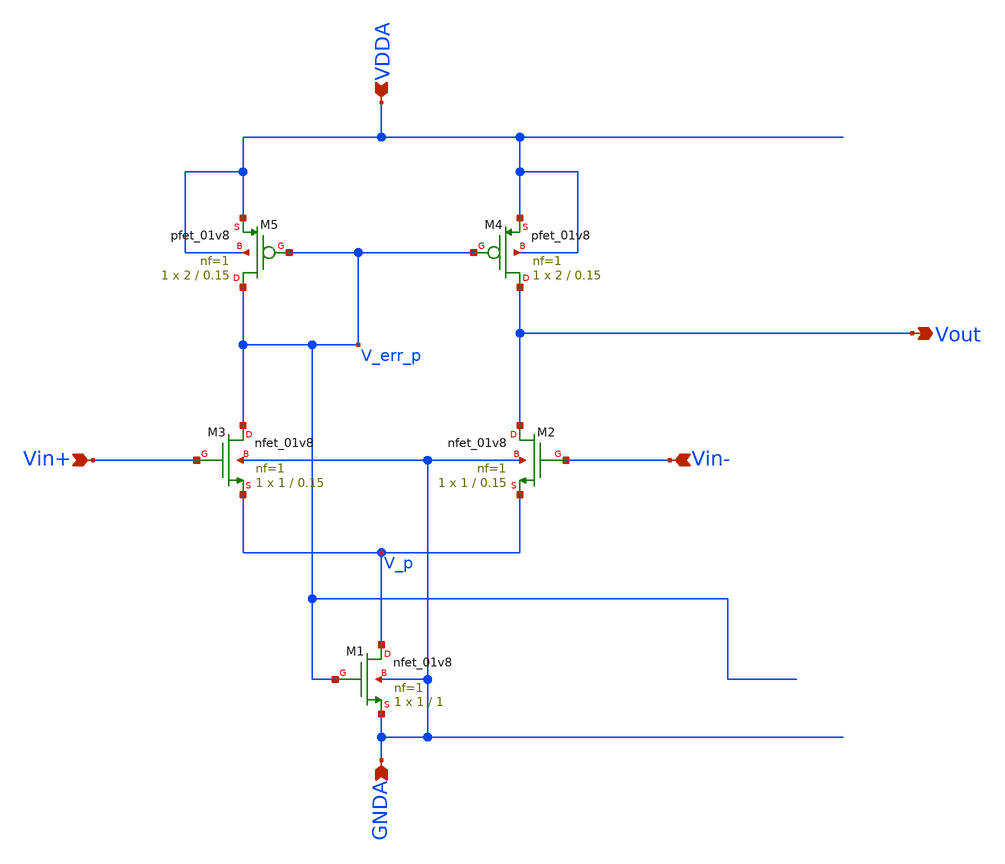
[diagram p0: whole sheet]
** sch_path: projects/bandgapref/xschem_ngspice/new_files/opamp_bandgap_4.sch
**.subckt opamp_bandgap_4 Vin+ Vout Vin- GNDA VDDA
*.ipin Vin+
*.opin Vout
*.ipin Vin-
*.ipin GNDA
*.ipin VDDA
XM4 Vout V_err_p VDDA VDDA sky130_fd_pr__pfet_01v8 L=0.15 W=2 nf=1 ad='int((nf+1)/2) * W/nf * 0.29' as='int((nf+2)/2) * W/nf * 0.29'
+ pd='2*int((nf+1)/2) * (W/nf + 0.29)' ps='2*int((nf+2)/2) * (W/nf + 0.29)' nrd='0.29 / W' nrs='0.29 / W'
+ sa=0 sb=0 sd=0 mult=1 m=1
XM5 V_err_p V_err_p VDDA VDDA sky130_fd_pr__pfet_01v8 L=0.15 W=2 nf=1 ad='int((nf+1)/2) * W/nf * 0.29'
+ as='int((nf+2)/2) * W/nf * 0.29' pd='2*int((nf+1)/2) * (W/nf + 0.29)' ps='2*int((nf+2)/2) * (W/nf + 0.29)'
+ nrd='0.29 / W' nrs='0.29 / W' sa=0 sb=0 sd=0 mult=1 m=1
XM2 Vout Vin- V_p GNDA sky130_fd_pr__nfet_01v8 L=0.15 W=1 nf=1 ad='int((nf+1)/2) * W/nf * 0.29' as='int((nf+2)/2) * W/nf * 0.29'
+ pd='2*int((nf+1)/2) * (W/nf + 0.29)' ps='2*int((nf+2)/2) * (W/nf + 0.29)' nrd='0.29 / W' nrs='0.29 / W'
+ sa=0 sb=0 sd=0 mult=1 m=1
XM3 V_err_p Vin+ V_p GNDA sky130_fd_pr__nfet_01v8 L=0.15 W=1 nf=1 ad='int((nf+1)/2) * W/nf * 0.29' as='int((nf+2)/2) * W/nf * 0.29'
+ pd='2*int((nf+1)/2) * (W/nf + 0.29)' ps='2*int((nf+2)/2) * (W/nf + 0.29)' nrd='0.29 / W' nrs='0.29 / W'
+ sa=0 sb=0 sd=0 mult=1 m=1
XM1 V_p V_err_p GNDA GNDA sky130_fd_pr__nfet_01v8 L=1 W=1 nf=1 ad='int((nf+1)/2) * W/nf * 0.29' as='int((nf+2)/2) * W/nf * 0.29'
+ pd='2*int((nf+1)/2) * (W/nf + 0.29)' ps='2*int((nf+2)/2) * (W/nf + 0.29)' nrd='0.29 / W' nrs='0.29 / W'
+ sa=0 sb=0 sd=0 mult=1 m=1
**.ends
.end
